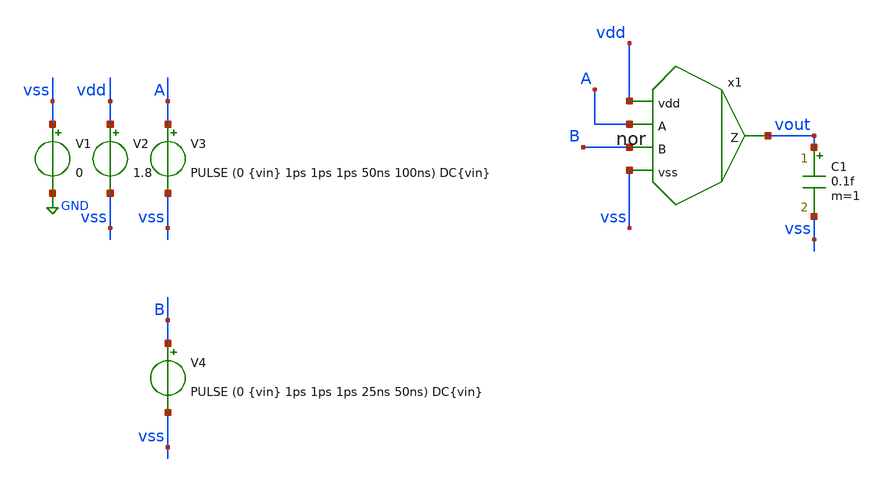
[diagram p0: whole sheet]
** sch_path: track_vlsi/lado/sch/tb_nor.sch
**.subckt tb_nor
V1 vss GND 0
V2 vdd vss 1.8
V3 A vss PULSE (0 {vin} 1ps 1ps 1ps 50ns 100ns) DC{vin}
C1 vout vss 0.1f m=1
V4 B vss PULSE (0 {vin} 1ps 1ps 1ps 25ns 50ns) DC{vin}
x1 vdd A B vout vss nor
**** begin user architecture code



*parametros
.param vin=1.8
.options TEMP=27.0

*include

.lib /home/eamta/skywater/skywater-pdk/libraries/sky130_fd_pr_ngspice/latest/models/corners/sky130.lib TT

*signals to save
.save all
*+ @m.x1.xm2.msky130_fd_pr__nfet_01v8[id] @m.x1.xm2.msky130_fd_pr__nfet_01v8[gm]
*+ @m.x1.xm1.msky130_fd_pr__pfet_01v8[id] @m.x1.xm1.msky130_fd_pr__pfet_01v8[gm]




*config simulacion

.control
  tran 0.1ns 0.5us
  setplot tran1
  plot v(vout) v(A) v(B)
  write tb_inverter_trans.raw
  gnuplot salida v(A) v(B) v(vout)
  reset
  dc V3 0 1.8 0.01
  setplot dc1
  plot v(vout) v(A) v(B)
  write tb_inverter_dc.raw
  reset
  op
  print all

.endc

.end


**** end user architecture code
**.ends

* expanding   symbol:  /home/eamta/eamta2021/sch/nor/nor.sym # of pins=5
** sym_path: track_vlsi/lado/sch/nor.sym
** sch_path: track_vlsi/lado/sch/nor.sch
.subckt nor vdd A B Z vss
*.opin Z
*.ipin vdd
*.ipin B
*.ipin vss
*.ipin A
XM1 net1 A vdd vdd sky130_fd_pr__pfet_01v8 L=0.15 W=0.9 nf=1 ad='int((nf+1)/2) * W/nf * 0.29' as='int((nf+2)/2) * W/nf * 0.29'
+ pd='2*int((nf+1)/2) * (W/nf + 0.29)' ps='2*int((nf+2)/2) * (W/nf + 0.29)' nrd='0.29 / W' nrs='0.29 / W'
+ sa=0 sb=0 sd=0 mult=1 m=1
XM2 Z B vss vss sky130_fd_pr__nfet_01v8 L=0.15 W=0.45 nf=1 ad='int((nf+1)/2) * W/nf * 0.29' as='int((nf+2)/2) * W/nf * 0.29'
+ pd='2*int((nf+1)/2) * (W/nf + 0.29)' ps='2*int((nf+2)/2) * (W/nf + 0.29)' nrd='0.29 / W' nrs='0.29 / W'
+ sa=0 sb=0 sd=0 mult=1 m=1
XM3 Z B net1 vdd sky130_fd_pr__pfet_01v8 L=0.15 W=0.9 nf=1 ad='int((nf+1)/2) * W/nf * 0.29' as='int((nf+2)/2) * W/nf * 0.29'
+ pd='2*int((nf+1)/2) * (W/nf + 0.29)' ps='2*int((nf+2)/2) * (W/nf + 0.29)' nrd='0.29 / W' nrs='0.29 / W'
+ sa=0 sb=0 sd=0 mult=1 m=1
XM4 Z A vss vss sky130_fd_pr__nfet_01v8 L=0.15 W=0.45 nf=1 ad='int((nf+1)/2) * W/nf * 0.29' as='int((nf+2)/2) * W/nf * 0.29'
+ pd='2*int((nf+1)/2) * (W/nf + 0.29)' ps='2*int((nf+2)/2) * (W/nf + 0.29)' nrd='0.29 / W' nrs='0.29 / W'
+ sa=0 sb=0 sd=0 mult=1 m=1
.ends

.GLOBAL GND
.end
